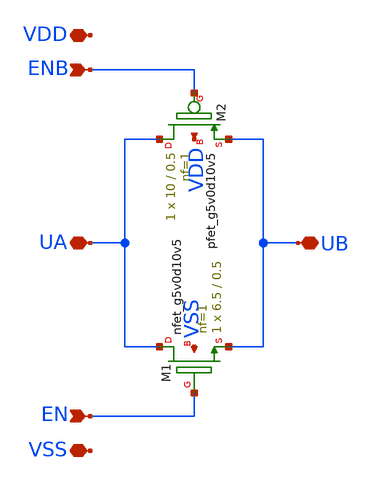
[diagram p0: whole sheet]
** sch_path: xschem/pass_gate.sch
**.subckt pass_gate VSS VDD UA UB EN ENB
*.iopin VSS
*.iopin VDD
*.iopin UA
*.iopin UB
*.ipin EN
*.ipin ENB
XM1 UA EN UB VSS sky130_fd_pr__nfet_g5v0d10v5 L=0.5 W=6.5 nf=1 ad='int((1 + 1)/2) * 6.5 / 1 * 0.29' as='int((1 + 2)/2) * 6.5 / 1 * 0.29'
+ pd='2*int((1 + 1)/2) * (6.5 / 1 + 0.29)' ps='2*int((1 + 2)/2) * (6.5 / 1 + 0.29)' nrd='0.29 / 6.5 ' nrs='0.29 / 6.5 '
+ sa=0 sb=0 sd=0 mult=1 m=1
XM2 UA ENB UB VDD sky130_fd_pr__pfet_g5v0d10v5 L=0.5 W=10 nf=1 ad='int((1 + 1)/2) * 10 / 1 * 0.29' as='int((1 + 2)/2) * 10 / 1 * 0.29'
+ pd='2*int((1 + 1)/2) * (10 / 1 + 0.29)' ps='2*int((1 + 2)/2) * (10 / 1 + 0.29)' nrd='0.29 / 10 ' nrs='0.29 / 10 '
+ sa=0 sb=0 sd=0 mult=1 m=1
**.ends
.end
